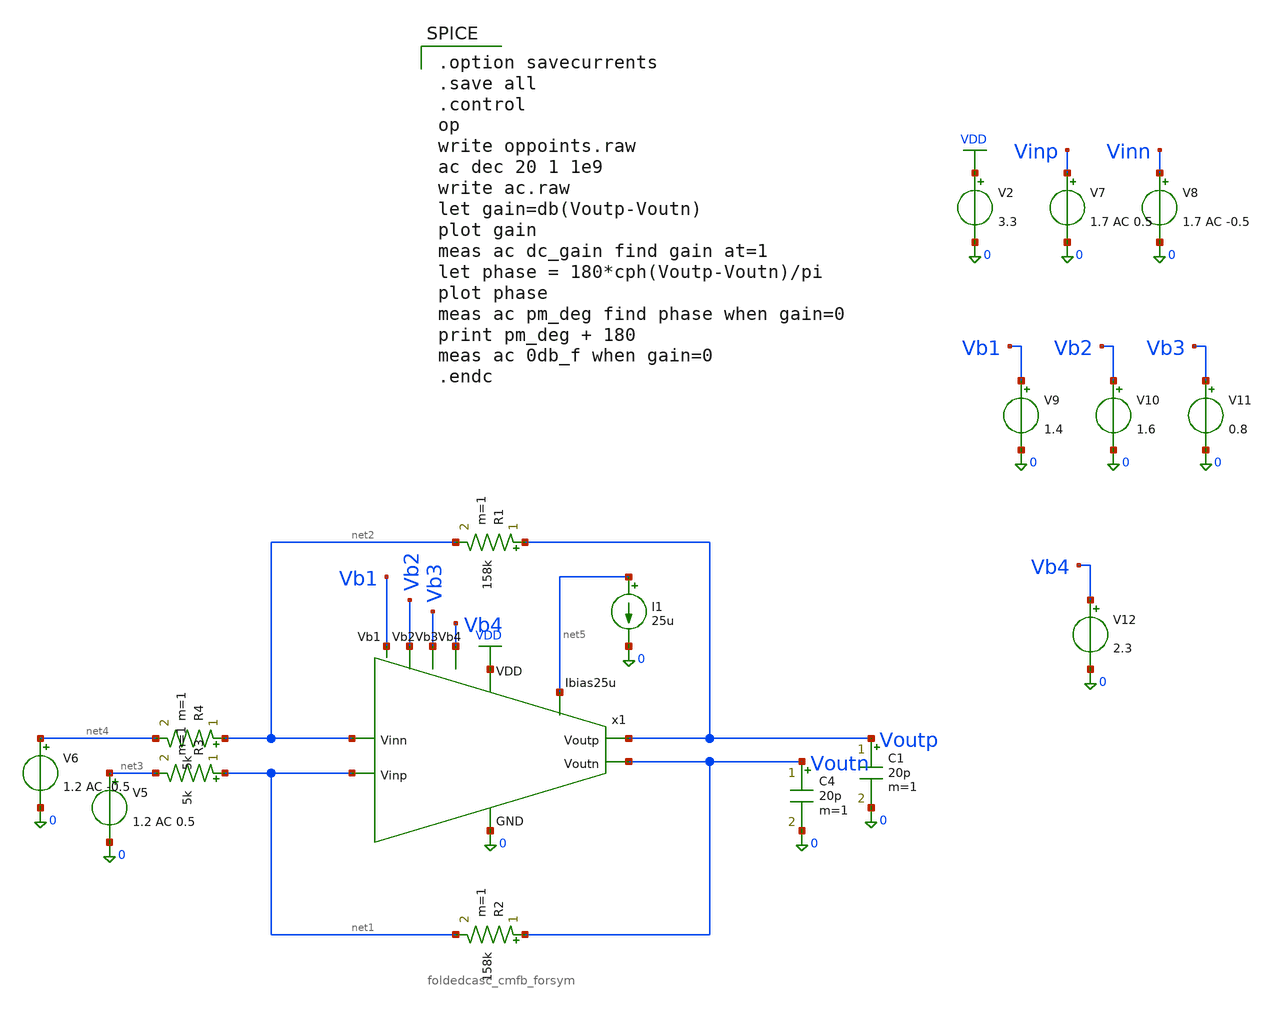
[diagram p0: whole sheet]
** sch_path: jz_fda2/fda2.sch
**.subckt fda2
C4 Voutn 0 20p m=1
C1 Voutp 0 20p m=1
I1 net5 0 25u
R1 Voutp net2 158k m=1
R2 Voutn net1 158k m=1
R3 net1 net3 5k m=1
R4 net2 net4 5k m=1
V5 net3 0 1.2 AC 0.5
V6 net4 0 1.2 AC -0.5
x1 VDD Vb2 Voutp Voutn Vb1 net5 net2 0 net1 Vb3 Vb4 foldedcasc_cmfb_forsym
V2 VDD 0 3.3
V7 Vinp 0 1.7 AC 0.5
V8 Vinn 0 1.7 AC -0.5
V9 Vb1 0 1.4
V10 Vb2 0 1.6
V11 Vb3 0 0.8
V12 Vb4 0 2.3
**** begin user architecture code

.option savecurrents
.save all
.control
op
write oppoints.raw
ac dec 20 1 1e9
write ac.raw
let gain=db(Voutp-Voutn)
plot gain
meas ac dc_gain find gain at=1
let phase = 180*cph(Voutp-Voutn)/pi
plot phase
meas ac pm_deg find phase when gain=0
print pm_deg + 180
meas ac 0db_f when gain=0
.endc


.include $::180MCU_MODELS/design.ngspice
.lib $::180MCU_MODELS/sm141064.ngspice typical
.lib $::180MCU_MODELS/smbb000149.ngspice typical

**** end user architecture code
**.ends

* expanding   symbol:  chipathon-2026-ppg/jz_fda2/foldedcasc_cmfb_forsym.sym # of pins=11
** sym_path: ps-filters/foldedcasc_cmfb_forsym.sym
** sch_path: ps-filters/foldedcasc_cmfb_forsym.sch
.subckt foldedcasc_cmfb_forsym VDD Vb2 Voutp Voutn Vb1 Ibias25u Vinn GND Vinp Vb3 Vb4
*.ipin VDD
*.opin Voutp
*.ipin Vinn
*.ipin Ibias25u
*.ipin GND
*.ipin Vinp
*.opin Voutn
*.ipin Vb4
*.ipin Vb1
*.ipin Vb2
*.ipin Vb3
XM5 net1 Vb3 GND GND nfet_03v3 L=0.28u W=13u nf=1 ad='int((nf+1)/2) * W/nf * 0.18u' as='int((nf+2)/2) * W/nf * 0.18u'
+ pd='2*int((nf+1)/2) * (W/nf + 0.18u)' ps='2*int((nf+2)/2) * (W/nf + 0.18u)' nrd='0.18u / W' nrs='0.18u / W'
+ sa=0 sb=0 sd=0 m=1
XM6 Voutn Vb2 net2 GND nfet_03v3 L=0.28u W=6.3u nf=1 ad='int((nf+1)/2) * W/nf * 0.18u' as='int((nf+2)/2) * W/nf * 0.18u'
+ pd='2*int((nf+1)/2) * (W/nf + 0.18u)' ps='2*int((nf+2)/2) * (W/nf + 0.18u)' nrd='0.18u / W' nrs='0.18u / W'
+ sa=0 sb=0 sd=0 m=1
XM7 Voutp Vb2 net1 GND nfet_03v3 L=0.28u W=6.3u nf=1 ad='int((nf+1)/2) * W/nf * 0.18u' as='int((nf+2)/2) * W/nf * 0.18u'
+ pd='2*int((nf+1)/2) * (W/nf + 0.18u)' ps='2*int((nf+2)/2) * (W/nf + 0.18u)' nrd='0.18u / W' nrs='0.18u / W'
+ sa=0 sb=0 sd=0 m=1
XM8 Voutn Vb1 net3 VDD pfet_03v3 L=0.28u W=19u nf=1 ad='int((nf+1)/2) * W/nf * 0.18u' as='int((nf+2)/2) * W/nf * 0.18u'
+ pd='2*int((nf+1)/2) * (W/nf + 0.18u)' ps='2*int((nf+2)/2) * (W/nf + 0.18u)' nrd='0.18u / W' nrs='0.18u / W'
+ sa=0 sb=0 sd=0 m=1
XM9 Voutp Vb1 net4 VDD pfet_03v3 L=0.28u W=19u nf=1 ad='int((nf+1)/2) * W/nf * 0.18u' as='int((nf+2)/2) * W/nf * 0.18u'
+ pd='2*int((nf+1)/2) * (W/nf + 0.18u)' ps='2*int((nf+2)/2) * (W/nf + 0.18u)' nrd='0.18u / W' nrs='0.18u / W'
+ sa=0 sb=0 sd=0 m=1
XM10 net3 Vb4 VDD VDD pfet_03v3 L=0.28u W=16.2u nf=1 ad='int((nf+1)/2) * W/nf * 0.18u' as='int((nf+2)/2) * W/nf * 0.18u'
+ pd='2*int((nf+1)/2) * (W/nf + 0.18u)' ps='2*int((nf+2)/2) * (W/nf + 0.18u)' nrd='0.18u / W' nrs='0.18u / W'
+ sa=0 sb=0 sd=0 m=1
XM11 net4 Vb4 VDD VDD pfet_03v3 L=0.28u W=16.2u nf=1 ad='int((nf+1)/2) * W/nf * 0.18u' as='int((nf+2)/2) * W/nf * 0.18u'
+ pd='2*int((nf+1)/2) * (W/nf + 0.18u)' ps='2*int((nf+2)/2) * (W/nf + 0.18u)' nrd='0.18u / W' nrs='0.18u / W'
+ sa=0 sb=0 sd=0 m=1
XM1 net1 Vinn net5 VDD pfet_03v3 L=0.28u W=3.45u nf=1 ad='int((nf+1)/2) * W/nf * 0.18u' as='int((nf+2)/2) * W/nf * 0.18u'
+ pd='2*int((nf+1)/2) * (W/nf + 0.18u)' ps='2*int((nf+2)/2) * (W/nf + 0.18u)' nrd='0.18u / W' nrs='0.18u / W'
+ sa=0 sb=0 sd=0 m=1
XM2 net2 Vinp net5 VDD pfet_03v3 L=0.28u W=3.45u nf=1 ad='int((nf+1)/2) * W/nf * 0.18u' as='int((nf+2)/2) * W/nf * 0.18u'
+ pd='2*int((nf+1)/2) * (W/nf + 0.18u)' ps='2*int((nf+2)/2) * (W/nf + 0.18u)' nrd='0.18u / W' nrs='0.18u / W'
+ sa=0 sb=0 sd=0 m=1
XM3 net5 Ibias25u net6 VDD pfet_03v3 L=0.28u W=4.9u nf=1 ad='int((nf+1)/2) * W/nf * 0.18u' as='int((nf+2)/2) * W/nf * 0.18u'
+ pd='2*int((nf+1)/2) * (W/nf + 0.18u)' ps='2*int((nf+2)/2) * (W/nf + 0.18u)' nrd='0.18u / W' nrs='0.18u / W'
+ sa=0 sb=0 sd=0 m=1
XM12 Ibias25u Ibias25u VDD VDD pfet_03v3 L=0.28u W=2.27u nf=1 ad='int((nf+1)/2) * W/nf * 0.18u' as='int((nf+2)/2) * W/nf * 0.18u'
+ pd='2*int((nf+1)/2) * (W/nf + 0.18u)' ps='2*int((nf+2)/2) * (W/nf + 0.18u)' nrd='0.18u / W' nrs='0.18u / W'
+ sa=0 sb=0 sd=0 m=1
XM13 net6 Voutp VDD VDD pfet_03v3 L=0.28u W=30u nf=1 ad='int((nf+1)/2) * W/nf * 0.18u' as='int((nf+2)/2) * W/nf * 0.18u'
+ pd='2*int((nf+1)/2) * (W/nf + 0.18u)' ps='2*int((nf+2)/2) * (W/nf + 0.18u)' nrd='0.18u / W' nrs='0.18u / W'
+ sa=0 sb=0 sd=0 m=1
XM14 net6 Voutn VDD VDD pfet_03v3 L=0.28u W=30u nf=1 ad='int((nf+1)/2) * W/nf * 0.18u' as='int((nf+2)/2) * W/nf * 0.18u'
+ pd='2*int((nf+1)/2) * (W/nf + 0.18u)' ps='2*int((nf+2)/2) * (W/nf + 0.18u)' nrd='0.18u / W' nrs='0.18u / W'
+ sa=0 sb=0 sd=0 m=1
XM4 net2 Vb3 GND GND nfet_03v3 L=0.28u W=13u nf=1 ad='int((nf+1)/2) * W/nf * 0.18u' as='int((nf+2)/2) * W/nf * 0.18u'
+ pd='2*int((nf+1)/2) * (W/nf + 0.18u)' ps='2*int((nf+2)/2) * (W/nf + 0.18u)' nrd='0.18u / W' nrs='0.18u / W'
+ sa=0 sb=0 sd=0 m=1
.ends

.GLOBAL VDD
.end
